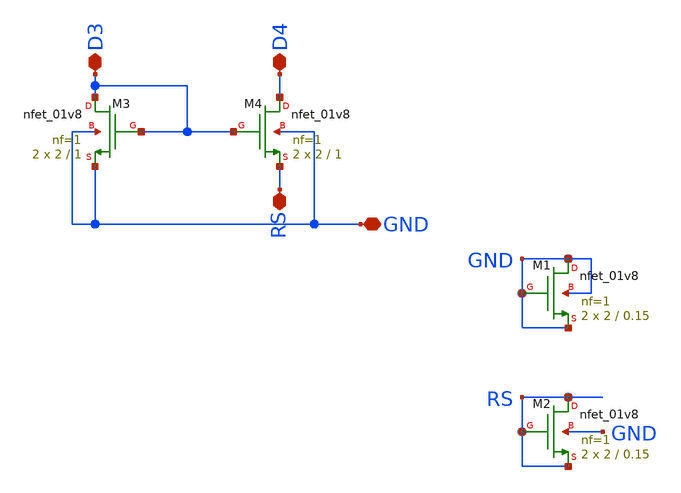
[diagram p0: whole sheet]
** sch_path: mag/nmoscs.sch
**.subckt nmoscs D3 D4 GND RS
*.iopin D3
*.iopin D4
*.iopin GND
*.iopin RS
XM4 D4 D3 RS GND sky130_fd_pr__nfet_01v8 L=1 W=2 nf=1 ad='int((nf+1)/2) * W/nf * 0.29' as='int((nf+2)/2) * W/nf * 0.29'
+ pd='2*int((nf+1)/2) * (W/nf + 0.29)' ps='2*int((nf+2)/2) * (W/nf + 0.29)' nrd='0.29 / W' nrs='0.29 / W'
+ sa=0 sb=0 sd=0 mult=2 m=2
XM3 D3 D3 GND GND sky130_fd_pr__nfet_01v8 L=1 W=2 nf=1 ad='int((nf+1)/2) * W/nf * 0.29' as='int((nf+2)/2) * W/nf * 0.29'
+ pd='2*int((nf+1)/2) * (W/nf + 0.29)' ps='2*int((nf+2)/2) * (W/nf + 0.29)' nrd='0.29 / W' nrs='0.29 / W'
+ sa=0 sb=0 sd=0 mult=2 m=2
XM1 GND GND GND GND sky130_fd_pr__nfet_01v8 L=0.15 W=2 nf=1 ad='int((nf+1)/2) * W/nf * 0.29' as='int((nf+2)/2) * W/nf * 0.29'
+ pd='2*int((nf+1)/2) * (W/nf + 0.29)' ps='2*int((nf+2)/2) * (W/nf + 0.29)' nrd='0.29 / W' nrs='0.29 / W'
+ sa=0 sb=0 sd=0 mult=2 m=2
XM2 RS RS RS GND sky130_fd_pr__nfet_01v8 L=0.15 W=2 nf=1 ad='int((nf+1)/2) * W/nf * 0.29' as='int((nf+2)/2) * W/nf * 0.29'
+ pd='2*int((nf+1)/2) * (W/nf + 0.29)' ps='2*int((nf+2)/2) * (W/nf + 0.29)' nrd='0.29 / W' nrs='0.29 / W'
+ sa=0 sb=0 sd=0 mult=2 m=2
**.ends
.end
